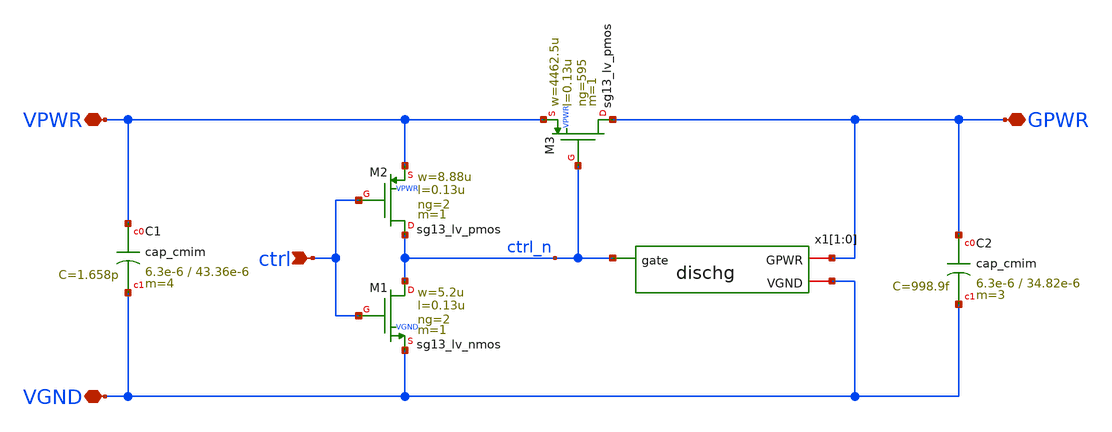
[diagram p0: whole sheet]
** sch_path: pg/ihp-sg13g2/tt_pg_1v5_hp_2/xschem/tt_pg_1v5_hp_2.sch
**.subckt tt_pg_1v5_hp_2 ctrl VPWR VGND GPWR
*.ipin ctrl
*.iopin VPWR
*.iopin VGND
*.iopin GPWR
XM1 ctrl_n ctrl VGND VGND sg13_lv_nmos w=5.2u l=0.13u ng=2 m=1
XM2 ctrl_n ctrl VPWR VPWR sg13_lv_pmos w=8.88u l=0.13u ng=2 m=1
XM3 GPWR ctrl_n VPWR VPWR sg13_lv_pmos w=4462.5u l=0.13u ng=595 m=1
XC1 VPWR VGND cap_cmim w=6.3e-6 l=43.36e-6 m=4 mm_ok=1
XC2 GPWR VGND cap_cmim w=6.3e-6 l=34.82e-6 m=3 mm_ok=1
x1[1] VGND GPWR ctrl_n dischg
x1[0] VGND GPWR ctrl_n dischg
**.ends

* expanding   symbol:  dischg.sym # of pins=3
** sym_path: pg/ihp-sg13g2/common/xschem/dischg.sym
** sch_path: pg/ihp-sg13g2/common/xschem/dischg.sch
.subckt dischg VGND GPWR gate
*.iopin GPWR
*.iopin VGND
*.ipin gate
XM1 GPWR gate net3 VGND sg13_lv_nmos w=0.50u l=0.65u ng=1 m=1
XM2 net3 gate net2 VGND sg13_lv_nmos w=0.50u l=0.65u ng=1 m=1
XM3 net2 gate net1 VGND sg13_lv_nmos w=0.50u l=0.65u ng=1 m=1
XM4 net1 gate VGND VGND sg13_lv_nmos w=0.50u l=0.65u ng=1 m=1
XM5 GPWR gate net6 VGND sg13_lv_nmos w=0.50u l=0.65u ng=1 m=1
XM6 net6 gate net5 VGND sg13_lv_nmos w=0.50u l=0.65u ng=1 m=1
XM7 net5 gate net4 VGND sg13_lv_nmos w=0.50u l=0.65u ng=1 m=1
XM8 net4 gate VGND VGND sg13_lv_nmos w=0.50u l=0.65u ng=1 m=1
.ends

.end
